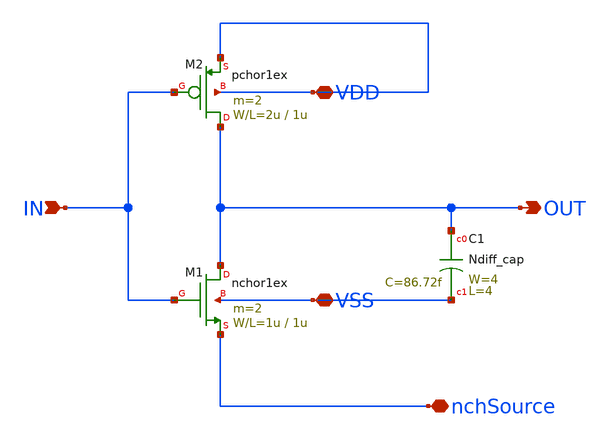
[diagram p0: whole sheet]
** sch_path: design/.design_bk/xschem/VCO/SA_VCO_INV.sch
**.subckt SA_VCO_INV nchSource IN OUT VDD VSS
*.iopin nchSource
*.ipin IN
*.opin OUT
*.iopin VDD
*.iopin VSS
M1 OUT IN nchSource VSS nchor1ex L=1u W=1u m=2
M2 OUT IN VDD VDD pchor1ex L=1u W=2u m=2
C1 OUT VSS Ndiff_cap W=4 L=4
**.ends
.end
